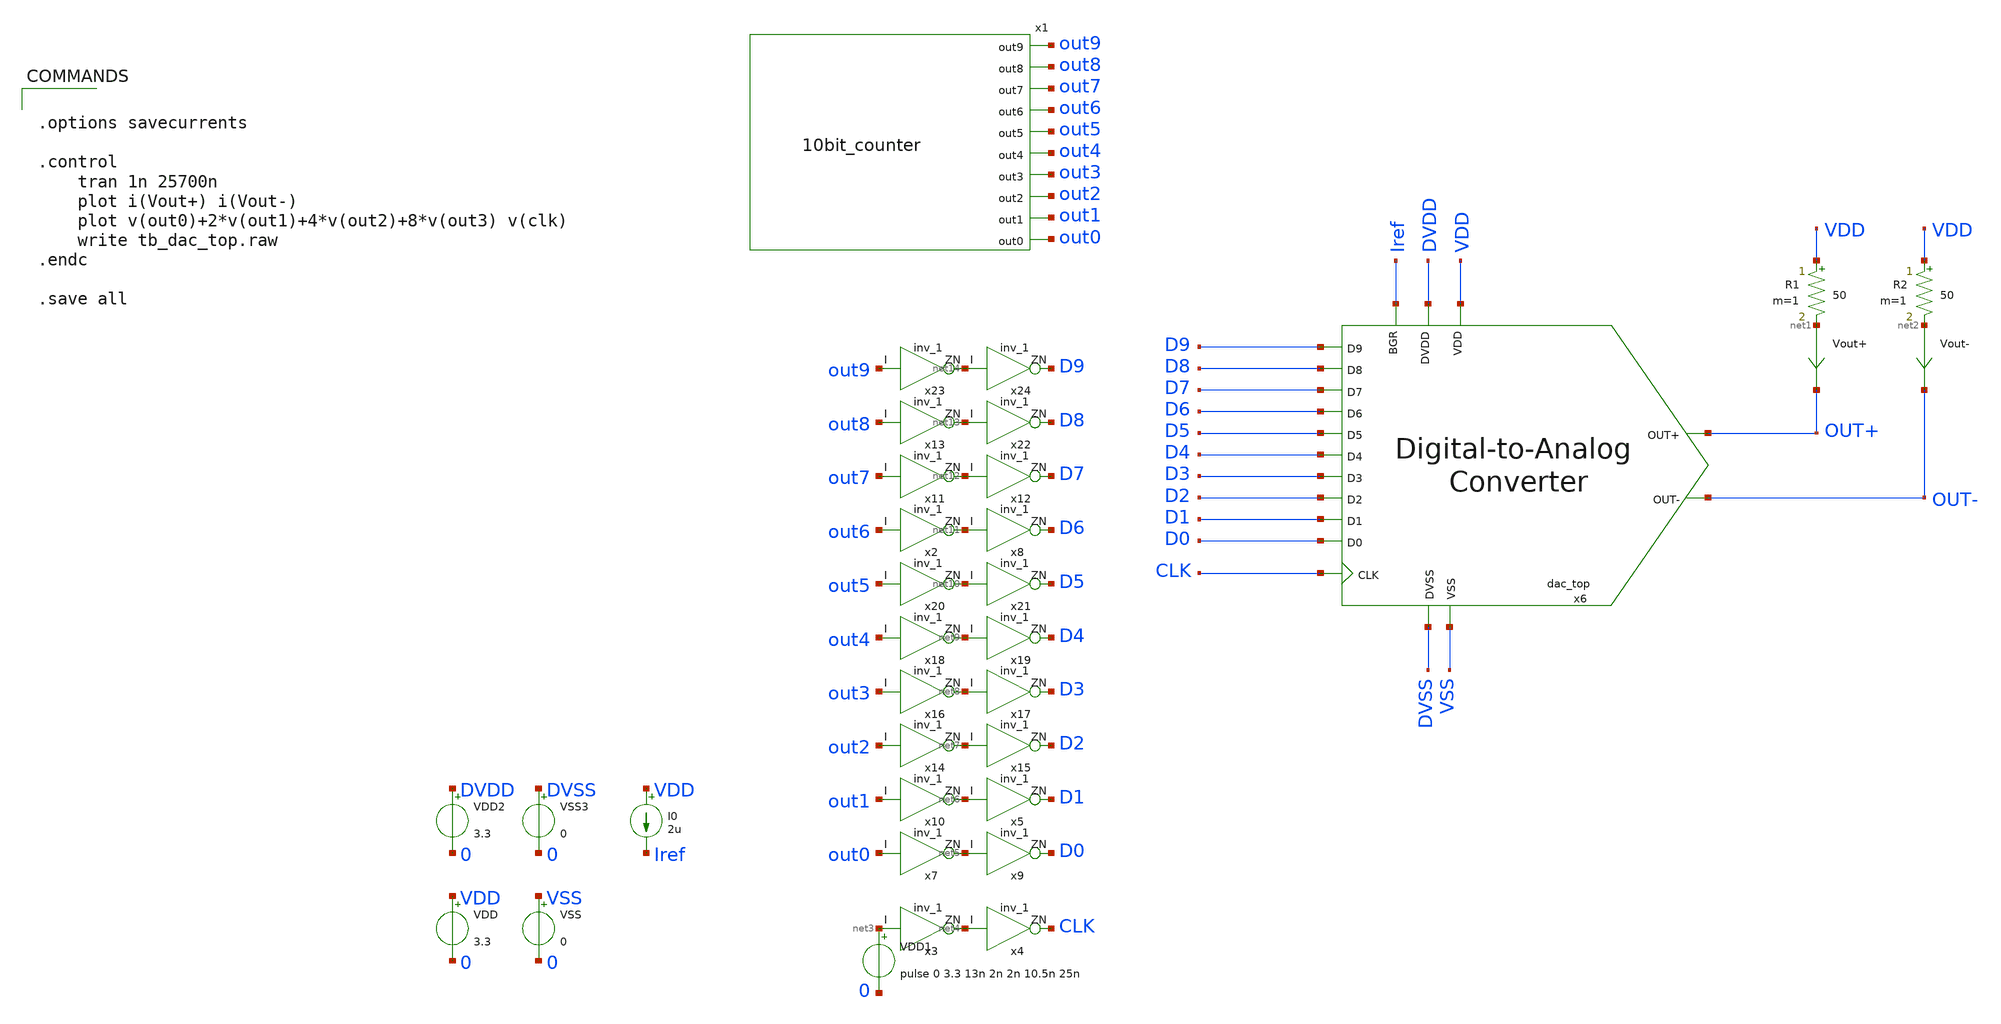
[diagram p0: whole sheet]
** sch_path: DAC/xschem/tb/tb_dac_top.sch
**.subckt tb_dac_top
VDD VDD 0 3.3
VSS VSS 0 0
VDD2 DVDD 0 3.3
VSS3 DVSS 0 0
I0 VDD Iref 2u
R1 VDD net1 50 m=1
R2 VDD net2 50 m=1
Vout+ net1 OUT+ 0
.save i(vout+)
Vout- net2 OUT- 0
.save i(vout-)
x6 D9 D8 D7 D6 D5 D4 D3 D2 D1 D0 CLK Iref VDD VSS OUT+ OUT- DVDD DVSS dac_top
x1 out0 out1 out2 out3 out4 out5 out6 out7 out8 out9 10bit_counter
VDD1 net3 0 pulse 0 3.3 13n 2n 2n 10.5n 25n
x3 net3 net4 DVDD DVDD DVSS DVSS gf180mcu_fd_sc_mcu7t5v0__inv_1
x4 net4 CLK DVDD DVDD DVSS DVSS gf180mcu_fd_sc_mcu7t5v0__inv_1
x7 out0 net5 DVDD DVDD DVSS DVSS gf180mcu_fd_sc_mcu7t5v0__inv_1
x9 net5 D0 DVDD DVDD DVSS DVSS gf180mcu_fd_sc_mcu7t5v0__inv_1
x10 out1 net6 DVDD DVDD DVSS DVSS gf180mcu_fd_sc_mcu7t5v0__inv_1
x5 net6 D1 DVDD DVDD DVSS DVSS gf180mcu_fd_sc_mcu7t5v0__inv_1
x14 out2 net7 DVDD DVDD DVSS DVSS gf180mcu_fd_sc_mcu7t5v0__inv_1
x15 net7 D2 DVDD DVDD DVSS DVSS gf180mcu_fd_sc_mcu7t5v0__inv_1
x16 out3 net8 DVDD DVDD DVSS DVSS gf180mcu_fd_sc_mcu7t5v0__inv_1
x17 net8 D3 DVDD DVDD DVSS DVSS gf180mcu_fd_sc_mcu7t5v0__inv_1
x18 out4 net9 DVDD DVDD DVSS DVSS gf180mcu_fd_sc_mcu7t5v0__inv_1
x19 net9 D4 DVDD DVDD DVSS DVSS gf180mcu_fd_sc_mcu7t5v0__inv_1
x20 out5 net10 DVDD DVDD DVSS DVSS gf180mcu_fd_sc_mcu7t5v0__inv_1
x21 net10 D5 DVDD DVDD DVSS DVSS gf180mcu_fd_sc_mcu7t5v0__inv_1
x2 out6 net11 DVDD DVDD DVSS DVSS gf180mcu_fd_sc_mcu7t5v0__inv_1
x8 net11 D6 DVDD DVDD DVSS DVSS gf180mcu_fd_sc_mcu7t5v0__inv_1
x11 out7 net12 DVDD DVDD DVSS DVSS gf180mcu_fd_sc_mcu7t5v0__inv_1
x12 net12 D7 DVDD DVDD DVSS DVSS gf180mcu_fd_sc_mcu7t5v0__inv_1
x13 out8 net13 DVDD DVDD DVSS DVSS gf180mcu_fd_sc_mcu7t5v0__inv_1
x22 net13 D8 DVDD DVDD DVSS DVSS gf180mcu_fd_sc_mcu7t5v0__inv_1
x23 out9 net14 DVDD DVDD DVSS DVSS gf180mcu_fd_sc_mcu7t5v0__inv_1
x24 net14 D9 DVDD DVDD DVSS DVSS gf180mcu_fd_sc_mcu7t5v0__inv_1
**** begin user architecture code


.options savecurrents

.control
    tran 1n 25700n
    plot i(Vout+) i(Vout-)
    plot v(out0)+2*v(out1)+4*v(out2)+8*v(out3) v(clk)
    write tb_dac_top.raw
.endc

.save all



.include /home/junbeom/pico/designs/xschem/dac_matrix_decoder.spice
.include $::180MCU_MODELS/design.ngspice
.lib $::180MCU_MODELS/sm141064.ngspice typical
.lib $::180MCU_MODELS/sm141064.ngspice res_typical
.lib $::180MCU_MODELS/sm141064.ngspice moscap_typical
.include $::180MCU_STDCELLS/spice/gf180mcu_fd_sc_mcu7t5v0.spice
*.lib $::180MCU_MODELS/sm141064.ngspice res_statistical

**** end user architecture code
**.ends
.end
